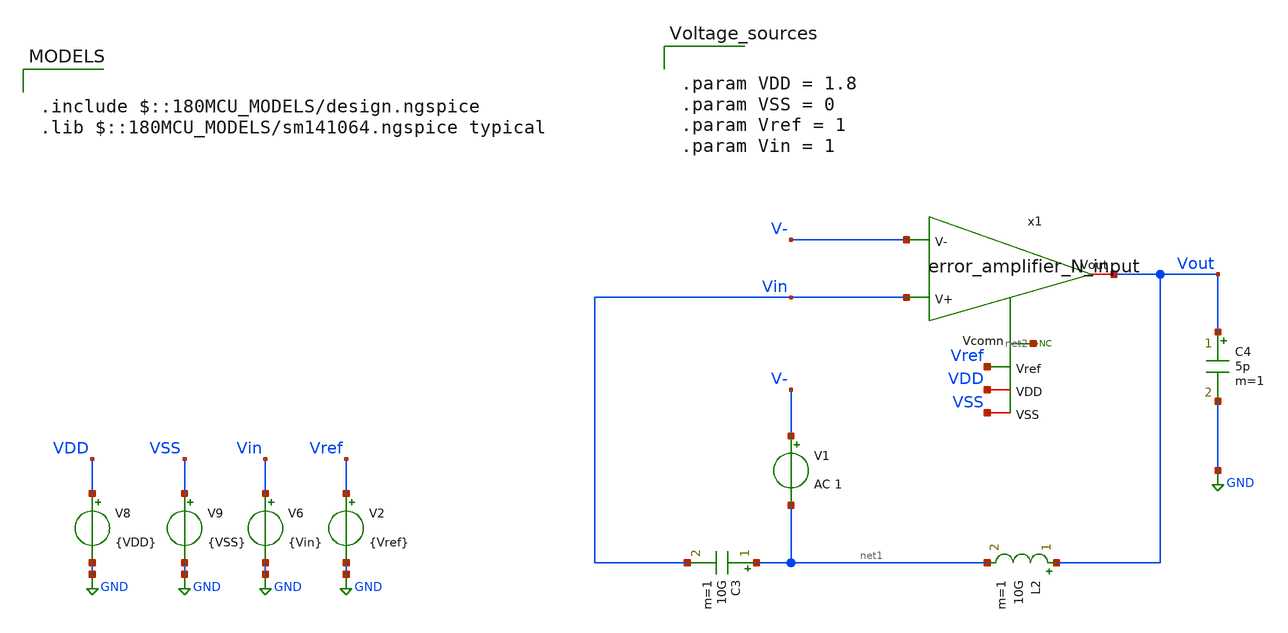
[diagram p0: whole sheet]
** sch_path: blocks/composite/folded_cascode/designs/gf180/error_amplifier_N_input/xschem/folded_cascode_ac.sch
**.subckt folded_cascode_ac
V1 V- net1 AC 1
C3 net1 Vin 10G m=1
L2 Vout net1 10G m=1
* noconn #net2
C4 Vout GND 5p m=1
V6 Vin GND {Vin}
V8 VDD GND {VDD}
V9 VSS GND {VSS}
x1 Vout Vin V- Vref VDD VSS net2 error_amplifier_N_input
V2 Vref GND {Vref}
**** begin user architecture code

.include $::180MCU_MODELS/design.ngspice
.lib $::180MCU_MODELS/sm141064.ngspice typical



.param VDD = 1.8
.param VSS = 0
.param Vref = 1
.param Vin = 1





.control
save all

** OP simulation
op

** run ac simulation
ac dec 20 1 100e6

** All OP parameters
setplot op1

let #####_M1_nmos_input_##### = 0
let id_M1 = @m.x1.x1.xm1.m0[id]
let gm_M1 = @m.x1.x1.xm1.m0[gm]
let ro_M1 = 1/@m.x1.x1.xm1.m0[gds]
let Vgs_M1 = @m.x1.x1.xm1.m0[vgs]
let Vds_M1 = @m.x1.x1.xm1.m0[vds]
let Vsb_M1 = -@m.x1.x1.xm1.m0[vbs]
let Vdsat_M1 = @m.x1.x1.xm1.m0[vdsat]
let Vth_M1 = @m.x1.x1.xm1.m0[vth]
let ao_M1 = gm_M1*ro_M1
let gmid_M1 = gm_M1/id_M1
let fT_M1 = gm_M1/(6.283185*@m.x1.x1.xm1.m0[cgg])
print #####_M1_nmos_input_##### id_M1 gm_M1 ro_M1 Vgs_M1 Vds_M1 Vsb_M1 Vdsat_M1 Vth_M1 ao_M1 gmid_M1
+ fT_M1

let #####_M2_nmos_input_##### = 0
let id_M2 = @m.x1.x1.xm2.m0[id]
let gm_M2 = @m.x1.x1.xm2.m0[gm]
let ro_M2 = 1/@m.x1.x1.xm2.m0[gds]
let Vgs_M2 = @m.x1.x1.xm2.m0[vgs]
let Vds_M2 = @m.x1.x1.xm2.m0[vds]
let Vsb_M2 = -@m.x1.x1.xm2.m0[vbs]
let Vdsat_M2 = @m.x1.x1.xm2.m0[vdsat]
let Vth_M2 = @m.x1.x1.xm2.m0[vth]
let ao_M2 = gm_M2*ro_M2
let gmid_M2 = gm_M2/id_M2
let fT_M2 = gm_M2/(6.283185*@m.x1.x1.xm2.m0[cgg])
print #####_M2_nmos_input_##### id_M2 gm_M2 ro_M2 Vgs_M2 Vds_M2 Vsb_M2 Vdsat_M2 Vth_M2 ao_M2 gmid_M2
+ fT_M2

let #####_M3_pmos_top_##### = 0
let id_M3 = @m.x1.x1.xm3.m0[id]
let gm_M3 = @m.x1.x1.xm3.m0[gm]
let ro_M3 = 1/@m.x1.x1.xm3.m0[gds]
let Vsg_M3 = @m.x1.x1.xm3.m0[vgs]
let Vsd_M3 = @m.x1.x1.xm3.m0[vds]
let Vbs_M3 = -@m.x1.x1.xm3.m0[vbs]
let Vdsat_M3 = @m.x1.x1.xm3.m0[vdsat]
let Vth_M3 = @m.x1.x1.xm3.m0[vth]
let ao_M3 = gm_M3*ro_M3
let gmid_M3 = gm_M3/id_M3
let fT_M3 = gm_M3/(6.283185*@m.x1.x1.xm3.m0[cgg])
print #####_M3_pmos_top_##### id_M3 gm_M3 ro_M3 Vsg_M3 Vsd_M3 Vbs_M3 Vdsat_M3 Vth_M3 ao_M3 gmid_M3
+ fT_M3

let #####_M4_pmos_top_##### = 0
let id_M4 = @m.x1.x1.xm4.m0[id]
let gm_M4 = @m.x1.x1.xm4.m0[gm]
let ro_M4 = 1/@m.x1.x1.xm4.m0[gds]
let Vsg_M4 = @m.x1.x1.xm4.m0[vgs]
let Vsd_M4 = @m.x1.x1.xm4.m0[vds]
let Vbs_M4 = -@m.x1.x1.xm4.m0[vbs]
let Vdsat_M4 = @m.x1.x1.xm4.m0[vdsat]
let Vth_M4 = @m.x1.x1.xm4.m0[vth]
let ao_M4 = gm_M4*ro_M4
let gmid_M4 = gm_M4/id_M4
let fT_M4 = gm_M4/(6.283185*@m.x1.x1.xm4.m0[cgg])
print #####_M4_pmos_top_##### id_M4 gm_M4 ro_M4 Vsg_M4 Vsd_M4 Vbs_M4 Vdsat_M4 Vth_M4 ao_M4 gmid_M4
+ fT_M4

let #####_M5_pmos_out_##### = 0
let id_M5 = @m.x1.x1.xm5.m0[id]
let gm_M5 = @m.x1.x1.xm5.m0[gm]
let ro_M5 = 1/@m.x1.x1.xm5.m0[gds]
let Vsg_M5 = @m.x1.x1.xm5.m0[vgs]
let Vsd_M5 = @m.x1.x1.xm5.m0[vds]
let Vbs_M5 = -@m.x1.x1.xm5.m0[vbs]
let Vdsat_M5 = @m.x1.x1.xm5.m0[vdsat]
let Vth_M5 = @m.x1.x1.xm5.m0[vth]
let ao_M5 = gm_M5*ro_M5
let gmid_M5 = gm_M5/id_M5
let fT_M5 = gm_M5/(6.283185*@m.x1.x1.xm5.m0[cgg])
print #####_M5_pmos_out_##### id_M5 gm_M5 ro_M5 Vsg_M5 Vsd_M5 Vbs_M5 Vdsat_M5 Vth_M5 ao_M5 gmid_M5
+ fT_M5

let #####_M6_pmos_out_##### = 0
let id_M6 = @m.x1.x1.xm6.m0[id]
let gm_M6 = @m.x1.x1.xm6.m0[gm]
let ro_M6 = 1/@m.x1.x1.xm6.m0[gds]
let Vsg_M6 = @m.x1.x1.xm6.m0[vgs]
let Vsd_M6 = @m.x1.x1.xm6.m0[vds]
let Vbs_M6 = -@m.x1.x1.xm6.m0[vbs]
let Vdsat_M6 = @m.x1.x1.xm6.m0[vdsat]
let Vth_M6 = @m.x1.x1.xm6.m0[vth]
let ao_M6 = gm_M6*ro_M6
let gmid_M6 = gm_M6/id_M6
let fT_M6 = gm_M6/(6.283185*@m.x1.x1.xm6.m0[cgg])
print #####_M6_pmos_out_##### id_M6 gm_M6 ro_M6 Vsg_M6 Vsd_M6 Vbs_M6 Vdsat_M6 Vth_M6 ao_M6 gmid_M6
+ fT_M6

let #####_M7_nmos_out_##### = 0
let id_M7 = @m.x1.x1.xm7.m0[id]
let gm_M7 = @m.x1.x1.xm7.m0[gm]
let ro_M7 = 1/@m.x1.x1.xm7.m0[gds]
let Vgs_M7 = @m.x1.x1.xm7.m0[vgs]
let Vds_M7 = @m.x1.x1.xm7.m0[vds]
let Vsb_M7 = -@m.x1.x1.xm7.m0[vbs]
let Vdsat_M7 = @m.x1.x1.xm7.m0[vdsat]
let Vth_M7 = @m.x1.x1.xm7.m0[vth]
let ao_M7 = gm_M7*ro_M7
let gmid_M7 = gm_M7/id_M7
let fT_M7 = gm_M7/(6.283185*@m.x1.x1.xm7.m0[cgg])
print #####_M7_nmos_out_##### id_M7 gm_M7 ro_M7 Vgs_M7 Vds_M7 Vsb_M7 Vdsat_M7 Vth_M7 ao_M7 gmid_M7
+ fT_M7

let #####_M8_nmos_out_##### = 0
let id_M8 = @m.x1.x1.xm8.m0[id]
let gm_M8 = @m.x1.x1.xm8.m0[gm]
let ro_M8 = 1/@m.x1.x1.xm8.m0[gds]
let Vgs_M8 = @m.x1.x1.xm8.m0[vgs]
let Vds_M8 = @m.x1.x1.xm8.m0[vds]
let Vsb_M8 = -@m.x1.x1.xm8.m0[vbs]
let Vdsat_M8 = @m.x1.x1.xm8.m0[vdsat]
let Vth_M8 = @m.x1.x1.xm8.m0[vth]
let ao_M8 = gm_M8*ro_M8
let gmid_M8 = gm_M8/id_M8
let fT_M8 = gm_M8/(6.283185*@m.x1.x1.xm8.m0[cgg])
print #####_M8_nmos_out_##### id_M8 gm_M8 ro_M8 Vgs_M8 Vds_M8 Vsb_M8 Vdsat_M8 Vth_M8 ao_M8 gmid_M8
+ fT_M8

let #####_M9_nmos_bottom_##### = 0
let id_M9 = @m.x1.x1.xm9.m0[id]
let gm_M9 = @m.x1.x1.xm9.m0[gm]
let ro_M9 = 1/@m.x1.x1.xm9.m0[gds]
let Vgs_M9 = @m.x1.x1.xm9.m0[vgs]
let Vds_M9 = @m.x1.x1.xm9.m0[vds]
let Vsb_M9 = -@m.x1.x1.xm9.m0[vbs]
let Vdsat_M9 = @m.x1.x1.xm9.m0[vdsat]
let Vth_M9 = @m.x1.x1.xm9.m0[vth]
let ao_M9 = gm_M9*ro_M9
let gmid_M9 = gm_M9/id_M9
let fT_M9 = gm_M9/(6.283185*@m.x1.x1.xm9.m0[cgg])
print #####_M9_nmos_bottom_##### id_M9 gm_M9 ro_M9 Vgs_M9 Vds_M9 Vsb_M9 Vdsat_M9 Vth_M9 ao_M9
+ gmid_M9 fT_M9

let #####_M10_nmos_bottom_##### = 0
let id_M10 = @m.x1.x1.xm10.m0[id]
let gm_M10 = @m.x1.x1.xm10.m0[gm]
let ro_M10 = 1/@m.x1.x1.xm10.m0[gds]
let Vgs_M10 = @m.x1.x1.xm10.m0[vgs]
let Vds_M10 = @m.x1.x1.xm10.m0[vds]
let Vsb_M10 = @m.x1.x1.xm10.m0[vbs]
let Vdsat_M10 = @m.x1.x1.xm10.m0[vdsat]
let Vth_M10 = @m.x1.x1.xm10.m0[vth]
let ao_M10 = gm_M10*ro_M10
let gmid_M10 = gm_M10/id_M10
let fT_M10 = gm_M10/(6.283185*@m.x1.x1.xm10.m0[cgg])
print #####_M10_nmos_bottom_##### id_M10 gm_M10 ro_M10 Vgs_M10 Vds_M10 Vsb_M10 Vdsat_M10 Vth_M10
+ ao_M10 gmid_M10 fT_M10

let #####_M11_nmos_mirror_##### = 0
let id_M11 = @m.x1.x1.xm11.m0[id]
let gm_M11 = @m.x1.x1.xm11.m0[gm]
let ro_M11 = 1/@m.x1.x1.xm11.m0[gds]
let Vgs_M11 = @m.x1.x1.xm11.m0[vgs]
let Vds_M11 = @m.x1.x1.xm11.m0[vds]
let Vsb_M11 = -@m.x1.x1.xm11.m0[vbs]
let Vdsat_M11 = @m.x1.x1.xm11.m0[vdsat]
let Vth_M11 = @m.x1.x1.xm11.m0[vth]
let ao_M11 = gm_M11*ro_M11
let gmid_M11 = gm_M11/id_M11
let fT_M11 = gm_M11/(6.283185*@m.x1.x1.xm11.m0[cgg])
print #####_M11_nmos_mirror_##### id_M11 gm_M11 ro_M11 Vgs_M11 Vds_M11 Vsb_M11 Vdsat_M11 Vth_M11
+ ao_M11 gmid_M11 fT_M11

** Custom output
let #####_Custom_output_##### = 0

* Power
let power = abs(i(V8))*VDD

* DC_gain
let r1 = ao_M6*ro_M4
let r2 = ao_M8*((ro_M1*ro_M10)/(ro_M1+ro_M10))
let Rout = (r1*r2)/(r1+r2)
let Av = db(gm_M1*Rout)
* Bandwidth
let BW = 1/(Rout*1e-12*6.283185)

print #####_Custom_output_##### Av BW Rout power gm_M1 ro_M1 gm_M6 ro_M6 ro_M4 gm_M8 ro_M8 ro_M10

write folded_cascode_ac.raw

setplot ac1

* measure parameters
let vout_mag = db(abs(v(Vout)))
let vout_phase = cph(v(Vout)) * 180/pi
let gm = (-1)*db(abs(v(Vout)))

meas ac A0 find vout_mag at=1e2
meas ac UGB when vout_mag=0 fall=1
meas ac PM find vout_phase when vout_mag=0
meas ac GM find gm when vout_phase=0

let A0_p1 = A0 - 3
meas ac BW when vout_mag=A0_p1

plot vout_mag vout_phase

.endc



**** end user architecture code
**.ends

* expanding   symbol:  gf180/error_amplifier_N_input/xschem/error_amplifier_N_input.sym # of pins=7
** sym_path: blocks/composite/folded_cascode/designs/gf180/error_amplifier_N_input/xschem/error_amplifier_N_input.sym
** sch_path: blocks/composite/folded_cascode/designs/gf180/error_amplifier_N_input/xschem/error_amplifier_N_input.sch
.subckt error_amplifier_N_input Vout V+ V- Vref VDD VSS Vcomn
*.ipin V+
*.iopin Vout
*.ipin V-
*.ipin Vref
*.iopin VDD
*.iopin VSS
*.iopin Vcomn
x1 VbiasP2 VbiasN2 VbiasN1 Vout V+ V- VDD VSS Vcomn error_amplifier_core_N_input
x2 VbiasN1 VbiasN2 VbiasP2 VDD VSS Vref net1 error_amplifier_bias_N_input
* noconn #net1
.ends


* expanding   symbol:  error_amplifier_core_N_input.sym # of pins=9
** sym_path: blocks/composite/folded_cascode/designs/gf180/error_amplifier_core_N_input/xschem/error_amplifier_core_N_input.sym
** sch_path: blocks/composite/folded_cascode/designs/gf180/error_amplifier_core_N_input/xschem/error_amplifier_core_N_input.sch
.subckt error_amplifier_core_N_input VbiasP2 VbiasN2 VbiasN1 Vout V+ V- VDD VSS Vcomn
*.ipin VbiasN2
*.iopin VDD
*.ipin VbiasP2
*.ipin VbiasN1
*.ipin V+
*.ipin V-
*.iopin VSS
*.iopin Vcomn
*.iopin Vout
XM4 Vdm6 Val VDD VDD pfet_03v3 L=0.3u W=4u nf=1 ad='int((nf+1)/2) * W/nf * 0.18u' as='int((nf+2)/2) * W/nf * 0.18u'
+ pd='2*int((nf+1)/2) * (W/nf + 0.18u)' ps='2*int((nf+2)/2) * (W/nf + 0.18u)' nrd='0.18u / W' nrs='0.18u / W'
+ sa=0 sb=0 sd=0 m=12
XM3 Vdm5 Val VDD VDD pfet_03v3 L=0.3u W=4u nf=1 ad='int((nf+1)/2) * W/nf * 0.18u' as='int((nf+2)/2) * W/nf * 0.18u'
+ pd='2*int((nf+1)/2) * (W/nf + 0.18u)' ps='2*int((nf+2)/2) * (W/nf + 0.18u)' nrd='0.18u / W' nrs='0.18u / W'
+ sa=0 sb=0 sd=0 m=12
XM5 Val VbiasP2 Vdm5 VDD pfet_03v3 L=2u W=6u nf=1 ad='int((nf+1)/2) * W/nf * 0.18u' as='int((nf+2)/2) * W/nf * 0.18u'
+ pd='2*int((nf+1)/2) * (W/nf + 0.18u)' ps='2*int((nf+2)/2) * (W/nf + 0.18u)' nrd='0.18u / W' nrs='0.18u / W'
+ sa=0 sb=0 sd=0 m=2
XM6 Vout VbiasP2 Vdm6 VDD pfet_03v3 L=2u W=6u nf=1 ad='int((nf+1)/2) * W/nf * 0.18u' as='int((nf+2)/2) * W/nf * 0.18u'
+ pd='2*int((nf+1)/2) * (W/nf + 0.18u)' ps='2*int((nf+2)/2) * (W/nf + 0.18u)' nrd='0.18u / W' nrs='0.18u / W'
+ sa=0 sb=0 sd=0 m=2
XM9 net1 VbiasN1 VSS VSS nfet_03v3 L=2u W=2u nf=1 ad='int((nf+1)/2) * W/nf * 0.18u' as='int((nf+2)/2) * W/nf * 0.18u'
+ pd='2*int((nf+1)/2) * (W/nf + 0.18u)' ps='2*int((nf+2)/2) * (W/nf + 0.18u)' nrd='0.18u / W' nrs='0.18u / W'
+ sa=0 sb=0 sd=0 m=2
XM8 Vout VbiasN2 Vcomn VSS nfet_03v3 L=2u W=5u nf=1 ad='int((nf+1)/2) * W/nf * 0.18u' as='int((nf+2)/2) * W/nf * 0.18u'
+ pd='2*int((nf+1)/2) * (W/nf + 0.18u)' ps='2*int((nf+2)/2) * (W/nf + 0.18u)' nrd='0.18u / W' nrs='0.18u / W'
+ sa=0 sb=0 sd=0 m=1
XM7 Val VbiasN2 net1 VSS nfet_03v3 L=2u W=5u nf=1 ad='int((nf+1)/2) * W/nf * 0.18u' as='int((nf+2)/2) * W/nf * 0.18u'
+ pd='2*int((nf+1)/2) * (W/nf + 0.18u)' ps='2*int((nf+2)/2) * (W/nf + 0.18u)' nrd='0.18u / W' nrs='0.18u / W'
+ sa=0 sb=0 sd=0 m=1
XM10 Vcomn VbiasN1 VSS VSS nfet_03v3 L=2u W=2u nf=1 ad='int((nf+1)/2) * W/nf * 0.18u' as='int((nf+2)/2) * W/nf * 0.18u'
+ pd='2*int((nf+1)/2) * (W/nf + 0.18u)' ps='2*int((nf+2)/2) * (W/nf + 0.18u)' nrd='0.18u / W' nrs='0.18u / W'
+ sa=0 sb=0 sd=0 m=2
XM15 VDD VDD VDD VDD pfet_03v3 L=3u W=1u nf=1 ad='int((nf+1)/2) * W/nf * 0.18u' as='int((nf+2)/2) * W/nf * 0.18u'
+ pd='2*int((nf+1)/2) * (W/nf + 0.18u)' ps='2*int((nf+2)/2) * (W/nf + 0.18u)' nrd='0.18u / W' nrs='0.18u / W'
+ sa=0 sb=0 sd=0 m=28
XM16 VDD VDD VDD VDD pfet_03v3 L=1.5u W=1u nf=1 ad='int((nf+1)/2) * W/nf * 0.18u' as='int((nf+2)/2) * W/nf * 0.18u'
+ pd='2*int((nf+1)/2) * (W/nf + 0.18u)' ps='2*int((nf+2)/2) * (W/nf + 0.18u)' nrd='0.18u / W' nrs='0.18u / W'
+ sa=0 sb=0 sd=0 m=20
XM13 VSS VSS VSS VSS nfet_03v3 L=3u W=1u nf=1 ad='int((nf+1)/2) * W/nf * 0.18u' as='int((nf+2)/2) * W/nf * 0.18u'
+ pd='2*int((nf+1)/2) * (W/nf + 0.18u)' ps='2*int((nf+2)/2) * (W/nf + 0.18u)' nrd='0.18u / W' nrs='0.18u / W'
+ sa=0 sb=0 sd=0 m=18
XM12 VSS VSS VSS VSS nfet_03v3 L=6.5u W=0.5u nf=1 ad='int((nf+1)/2) * W/nf * 0.18u' as='int((nf+2)/2) * W/nf * 0.18u'
+ pd='2*int((nf+1)/2) * (W/nf + 0.18u)' ps='2*int((nf+2)/2) * (W/nf + 0.18u)' nrd='0.18u / W' nrs='0.18u / W'
+ sa=0 sb=0 sd=0 m=36
XM14 VSS VSS VSS VSS nfet_03v3 L=1u W=1u nf=1 ad='int((nf+1)/2) * W/nf * 0.18u' as='int((nf+2)/2) * W/nf * 0.18u'
+ pd='2*int((nf+1)/2) * (W/nf + 0.18u)' ps='2*int((nf+2)/2) * (W/nf + 0.18u)' nrd='0.18u / W' nrs='0.18u / W'
+ sa=0 sb=0 sd=0 m=30
XM1 Vdm6 V- net2 VSS nfet_03v3 L=1u W=10u nf=1 ad='int((nf+1)/2) * W/nf * 0.18u' as='int((nf+2)/2) * W/nf * 0.18u'
+ pd='2*int((nf+1)/2) * (W/nf + 0.18u)' ps='2*int((nf+2)/2) * (W/nf + 0.18u)' nrd='0.18u / W' nrs='0.18u / W'
+ sa=0 sb=0 sd=0 m=20
XM2 Vdm5 V+ net2 VSS nfet_03v3 L=1u W=10u nf=1 ad='int((nf+1)/2) * W/nf * 0.18u' as='int((nf+2)/2) * W/nf * 0.18u'
+ pd='2*int((nf+1)/2) * (W/nf + 0.18u)' ps='2*int((nf+2)/2) * (W/nf + 0.18u)' nrd='0.18u / W' nrs='0.18u / W'
+ sa=0 sb=0 sd=0 m=20
XM11 net2 VbiasN1 VSS VSS nfet_03v3 L=2u W=2u nf=1 ad='int((nf+1)/2) * W/nf * 0.18u' as='int((nf+2)/2) * W/nf * 0.18u'
+ pd='2*int((nf+1)/2) * (W/nf + 0.18u)' ps='2*int((nf+2)/2) * (W/nf + 0.18u)' nrd='0.18u / W' nrs='0.18u / W'
+ sa=0 sb=0 sd=0 m=40
.ends


* expanding   symbol:  error_amplifier_bias_N_input.sym # of pins=7
** sym_path: blocks/composite/folded_cascode/designs/gf180/error_amplifier_bias_N_input/xschem/error_amplifier_bias_N_input.sym
** sch_path: blocks/composite/folded_cascode/designs/gf180/error_amplifier_bias_N_input/xschem/error_amplifier_bias_N_input.sch
.subckt error_amplifier_bias_N_input VbiasN1 VbiasN2 VbiasP2 VDD VSS Vref VbiasP1
*.ipin Vref
*.iopin VbiasN1
*.iopin VbiasN2
*.iopin VDD
*.iopin VbiasP2
*.iopin VSS
*.iopin VbiasP1
XM1 VbiasN2 VbiasN2 net2 VSS nfet_03v3 L=6u W=0.5u nf=1 ad='int((nf+1)/2) * W/nf * 0.18u' as='int((nf+2)/2) * W/nf * 0.18u'
+ pd='2*int((nf+1)/2) * (W/nf + 0.18u)' ps='2*int((nf+2)/2) * (W/nf + 0.18u)' nrd='0.18u / W' nrs='0.18u / W'
+ sa=0 sb=0 sd=0 m=1
XM2 VbiasP1 VbiasP1 VDD VDD pfet_03v3 L=2u W=0.5u nf=1 ad='int((nf+1)/2) * W/nf * 0.18u' as='int((nf+2)/2) * W/nf * 0.18u'
+ pd='2*int((nf+1)/2) * (W/nf + 0.18u)' ps='2*int((nf+2)/2) * (W/nf + 0.18u)' nrd='0.18u / W' nrs='0.18u / W'
+ sa=0 sb=0 sd=0 m=1
XM3 VbiasP1 Vref net1 VSS nfet_03v3 L=6u W=0.5u nf=1 ad='int((nf+1)/2) * W/nf * 0.18u' as='int((nf+2)/2) * W/nf * 0.18u'
+ pd='2*int((nf+1)/2) * (W/nf + 0.18u)' ps='2*int((nf+2)/2) * (W/nf + 0.18u)' nrd='0.18u / W' nrs='0.18u / W'
+ sa=0 sb=0 sd=0 m=1
XM4 VbiasN2 VbiasP1 VDD VDD pfet_03v3 L=2u W=0.5u nf=1 ad='int((nf+1)/2) * W/nf * 0.18u' as='int((nf+2)/2) * W/nf * 0.18u'
+ pd='2*int((nf+1)/2) * (W/nf + 0.18u)' ps='2*int((nf+2)/2) * (W/nf + 0.18u)' nrd='0.18u / W' nrs='0.18u / W'
+ sa=0 sb=0 sd=0 m=1
XM5 VbiasN1 VbiasP1 VDD VDD pfet_03v3 L=2u W=0.5u nf=1 ad='int((nf+1)/2) * W/nf * 0.18u' as='int((nf+2)/2) * W/nf * 0.18u'
+ pd='2*int((nf+1)/2) * (W/nf + 0.18u)' ps='2*int((nf+2)/2) * (W/nf + 0.18u)' nrd='0.18u / W' nrs='0.18u / W'
+ sa=0 sb=0 sd=0 m=1
XM6 net6 VbiasP2 VDD VDD pfet_03v3 L=2u W=0.5u nf=1 ad='int((nf+1)/2) * W/nf * 0.18u' as='int((nf+2)/2) * W/nf * 0.18u'
+ pd='2*int((nf+1)/2) * (W/nf + 0.18u)' ps='2*int((nf+2)/2) * (W/nf + 0.18u)' nrd='0.18u / W' nrs='0.18u / W'
+ sa=0 sb=0 sd=0 m=1
XM7 VbiasP2 VbiasP2 net6 VDD pfet_03v3 L=2u W=0.5u nf=1 ad='int((nf+1)/2) * W/nf * 0.18u' as='int((nf+2)/2) * W/nf * 0.18u'
+ pd='2*int((nf+1)/2) * (W/nf + 0.18u)' ps='2*int((nf+2)/2) * (W/nf + 0.18u)' nrd='0.18u / W' nrs='0.18u / W'
+ sa=0 sb=0 sd=0 m=1
XM8 net7 net8 VDD VDD pfet_03v3 L=2u W=0.5u nf=1 ad='int((nf+1)/2) * W/nf * 0.18u' as='int((nf+2)/2) * W/nf * 0.18u'
+ pd='2*int((nf+1)/2) * (W/nf + 0.18u)' ps='2*int((nf+2)/2) * (W/nf + 0.18u)' nrd='0.18u / W' nrs='0.18u / W'
+ sa=0 sb=0 sd=0 m=3
XM9 net8 VbiasP2 net7 VDD pfet_03v3 L=2u W=0.5u nf=1 ad='int((nf+1)/2) * W/nf * 0.18u' as='int((nf+2)/2) * W/nf * 0.18u'
+ pd='2*int((nf+1)/2) * (W/nf + 0.18u)' ps='2*int((nf+2)/2) * (W/nf + 0.18u)' nrd='0.18u / W' nrs='0.18u / W'
+ sa=0 sb=0 sd=0 m=2
XM10 net10 VbiasN1 VSS VSS nfet_03v3 L=6u W=0.5u nf=1 ad='int((nf+1)/2) * W/nf * 0.18u' as='int((nf+2)/2) * W/nf * 0.18u'
+ pd='2*int((nf+1)/2) * (W/nf + 0.18u)' ps='2*int((nf+2)/2) * (W/nf + 0.18u)' nrd='0.18u / W' nrs='0.18u / W'
+ sa=0 sb=0 sd=0 m=4
XM11 VbiasN1 VbiasN2 net3 VSS nfet_03v3 L=6u W=0.5u nf=1 ad='int((nf+1)/2) * W/nf * 0.18u' as='int((nf+2)/2) * W/nf * 0.18u'
+ pd='2*int((nf+1)/2) * (W/nf + 0.18u)' ps='2*int((nf+2)/2) * (W/nf + 0.18u)' nrd='0.18u / W' nrs='0.18u / W'
+ sa=0 sb=0 sd=0 m=5
XM12 VbiasP2 VbiasN2 net4 VSS nfet_03v3 L=6u W=0.5u nf=1 ad='int((nf+1)/2) * W/nf * 0.18u' as='int((nf+2)/2) * W/nf * 0.18u'
+ pd='2*int((nf+1)/2) * (W/nf + 0.18u)' ps='2*int((nf+2)/2) * (W/nf + 0.18u)' nrd='0.18u / W' nrs='0.18u / W'
+ sa=0 sb=0 sd=0 m=5
XM13 net8 VbiasN2 net9 VSS nfet_03v3 L=6u W=0.5u nf=1 ad='int((nf+1)/2) * W/nf * 0.18u' as='int((nf+2)/2) * W/nf * 0.18u'
+ pd='2*int((nf+1)/2) * (W/nf + 0.18u)' ps='2*int((nf+2)/2) * (W/nf + 0.18u)' nrd='0.18u / W' nrs='0.18u / W'
+ sa=0 sb=0 sd=0 m=5
XM14 net2 VbiasN2 VSS VSS nfet_03v3 L=6u W=0.5u nf=1 ad='int((nf+1)/2) * W/nf * 0.18u' as='int((nf+2)/2) * W/nf * 0.18u'
+ pd='2*int((nf+1)/2) * (W/nf + 0.18u)' ps='2*int((nf+2)/2) * (W/nf + 0.18u)' nrd='0.18u / W' nrs='0.18u / W'
+ sa=0 sb=0 sd=0 m=1
XM15 net3 VbiasN1 net11 VSS nfet_03v3 L=6u W=0.5u nf=1 ad='int((nf+1)/2) * W/nf * 0.18u' as='int((nf+2)/2) * W/nf * 0.18u'
+ pd='2*int((nf+1)/2) * (W/nf + 0.18u)' ps='2*int((nf+2)/2) * (W/nf + 0.18u)' nrd='0.18u / W' nrs='0.18u / W'
+ sa=0 sb=0 sd=0 m=4
XM16 net4 VbiasN1 net5 VSS nfet_03v3 L=6u W=0.5u nf=1 ad='int((nf+1)/2) * W/nf * 0.18u' as='int((nf+2)/2) * W/nf * 0.18u'
+ pd='2*int((nf+1)/2) * (W/nf + 0.18u)' ps='2*int((nf+2)/2) * (W/nf + 0.18u)' nrd='0.18u / W' nrs='0.18u / W'
+ sa=0 sb=0 sd=0 m=4
XM17 net9 VbiasN1 net10 VSS nfet_03v3 L=6u W=0.5u nf=1 ad='int((nf+1)/2) * W/nf * 0.18u' as='int((nf+2)/2) * W/nf * 0.18u'
+ pd='2*int((nf+1)/2) * (W/nf + 0.18u)' ps='2*int((nf+2)/2) * (W/nf + 0.18u)' nrd='0.18u / W' nrs='0.18u / W'
+ sa=0 sb=0 sd=0 m=4
XM18 net1 Vref VSS VSS nfet_03v3 L=6u W=0.5u nf=1 ad='int((nf+1)/2) * W/nf * 0.18u' as='int((nf+2)/2) * W/nf * 0.18u'
+ pd='2*int((nf+1)/2) * (W/nf + 0.18u)' ps='2*int((nf+2)/2) * (W/nf + 0.18u)' nrd='0.18u / W' nrs='0.18u / W'
+ sa=0 sb=0 sd=0 m=1
XM19 net5 VbiasN1 VSS VSS nfet_03v3 L=6u W=0.5u nf=1 ad='int((nf+1)/2) * W/nf * 0.18u' as='int((nf+2)/2) * W/nf * 0.18u'
+ pd='2*int((nf+1)/2) * (W/nf + 0.18u)' ps='2*int((nf+2)/2) * (W/nf + 0.18u)' nrd='0.18u / W' nrs='0.18u / W'
+ sa=0 sb=0 sd=0 m=4
XM20 net11 VbiasN1 VSS VSS nfet_03v3 L=6u W=0.5u nf=1 ad='int((nf+1)/2) * W/nf * 0.18u' as='int((nf+2)/2) * W/nf * 0.18u'
+ pd='2*int((nf+1)/2) * (W/nf + 0.18u)' ps='2*int((nf+2)/2) * (W/nf + 0.18u)' nrd='0.18u / W' nrs='0.18u / W'
+ sa=0 sb=0 sd=0 m=4
.ends

.GLOBAL GND
.end
